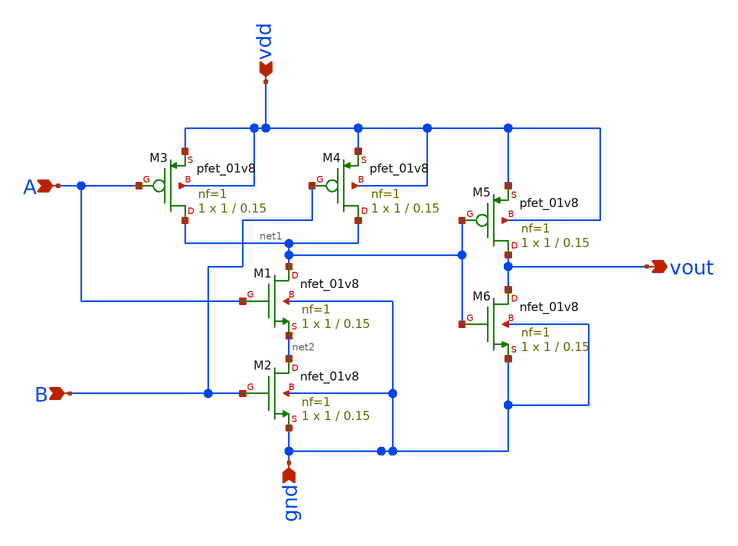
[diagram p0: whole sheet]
** sch_path: and.sch
**.subckt and A B gnd vdd vout
*.ipin A
*.ipin B
*.ipin gnd
*.ipin vdd
*.opin vout
XM1 net1 A net2 gnd sky130_fd_pr__nfet_01v8 L=0.15 W=1 nf=1 ad='int((nf+1)/2) * W/nf * 0.29' as='int((nf+2)/2) * W/nf * 0.29'
+ pd='2*int((nf+1)/2) * (W/nf + 0.29)' ps='2*int((nf+2)/2) * (W/nf + 0.29)' nrd='0.29 / W' nrs='0.29 / W'
+ sa=0 sb=0 sd=0 mult=1 m=1
XM2 net2 B gnd gnd sky130_fd_pr__nfet_01v8 L=0.15 W=1 nf=1 ad='int((nf+1)/2) * W/nf * 0.29' as='int((nf+2)/2) * W/nf * 0.29'
+ pd='2*int((nf+1)/2) * (W/nf + 0.29)' ps='2*int((nf+2)/2) * (W/nf + 0.29)' nrd='0.29 / W' nrs='0.29 / W'
+ sa=0 sb=0 sd=0 mult=1 m=1
XM3 net1 A vdd vdd sky130_fd_pr__pfet_01v8 L=0.15 W=1 nf=1 ad='int((nf+1)/2) * W/nf * 0.29' as='int((nf+2)/2) * W/nf * 0.29'
+ pd='2*int((nf+1)/2) * (W/nf + 0.29)' ps='2*int((nf+2)/2) * (W/nf + 0.29)' nrd='0.29 / W' nrs='0.29 / W'
+ sa=0 sb=0 sd=0 mult=1 m=1
XM4 net1 B vdd vdd sky130_fd_pr__pfet_01v8 L=0.15 W=1 nf=1 ad='int((nf+1)/2) * W/nf * 0.29' as='int((nf+2)/2) * W/nf * 0.29'
+ pd='2*int((nf+1)/2) * (W/nf + 0.29)' ps='2*int((nf+2)/2) * (W/nf + 0.29)' nrd='0.29 / W' nrs='0.29 / W'
+ sa=0 sb=0 sd=0 mult=1 m=1
XM5 vout net1 vdd vdd sky130_fd_pr__pfet_01v8 L=0.15 W=1 nf=1 ad='int((nf+1)/2) * W/nf * 0.29' as='int((nf+2)/2) * W/nf * 0.29'
+ pd='2*int((nf+1)/2) * (W/nf + 0.29)' ps='2*int((nf+2)/2) * (W/nf + 0.29)' nrd='0.29 / W' nrs='0.29 / W'
+ sa=0 sb=0 sd=0 mult=1 m=1
XM6 vout net1 gnd gnd sky130_fd_pr__nfet_01v8 L=0.15 W=1 nf=1 ad='int((nf+1)/2) * W/nf * 0.29' as='int((nf+2)/2) * W/nf * 0.29'
+ pd='2*int((nf+1)/2) * (W/nf + 0.29)' ps='2*int((nf+2)/2) * (W/nf + 0.29)' nrd='0.29 / W' nrs='0.29 / W'
+ sa=0 sb=0 sd=0 mult=1 m=1
**.ends
.end
